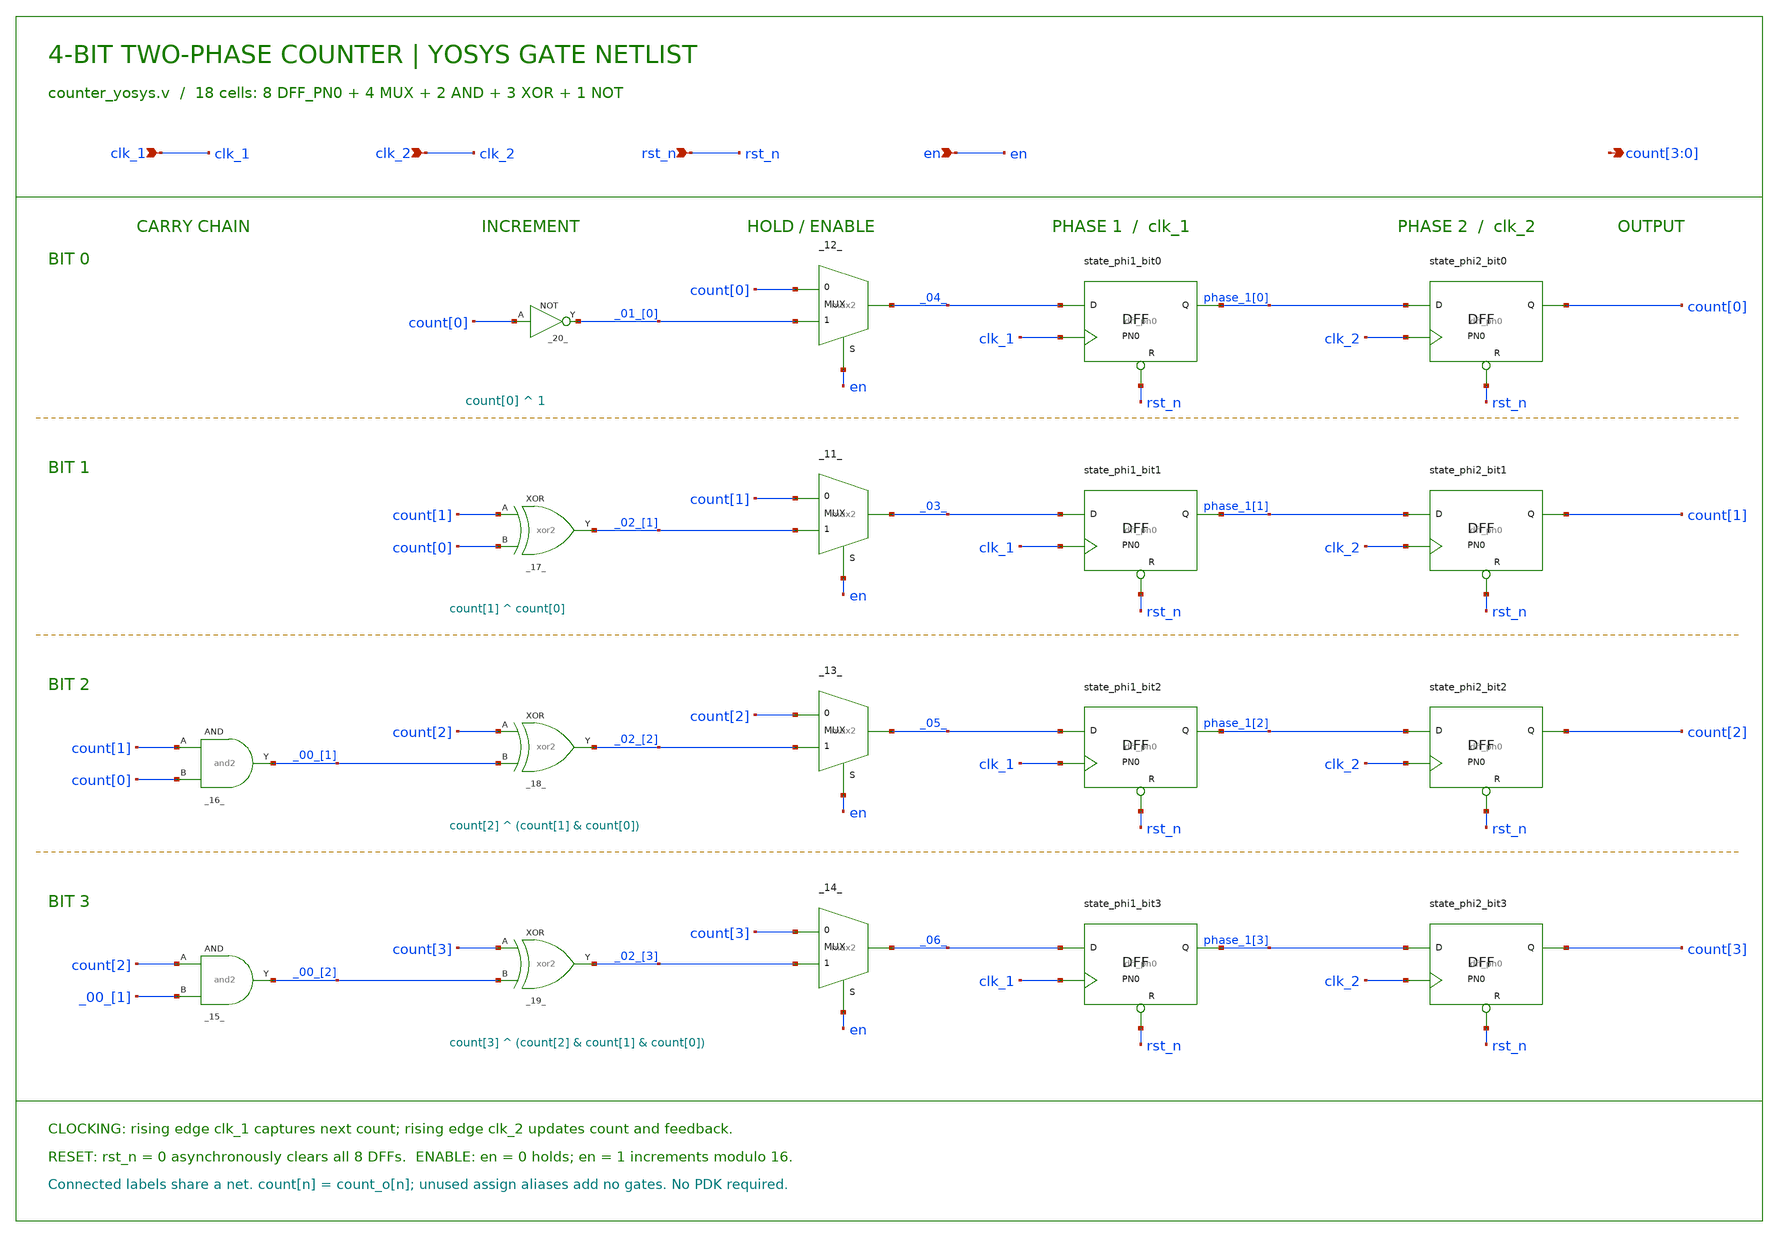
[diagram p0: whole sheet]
** sch_path: examples/counter/counter_latch_mux_1/counter_yosys.sch
**.subckt counter_yosys clk_1 clk_2 rst_n en count[3],count[2],count[1],count[0]
*.ipin clk_1
*.ipin clk_2
*.ipin rst_n
*.ipin en
*.opin count[3],count[2],count[1],count[0]
**.ends
.end
